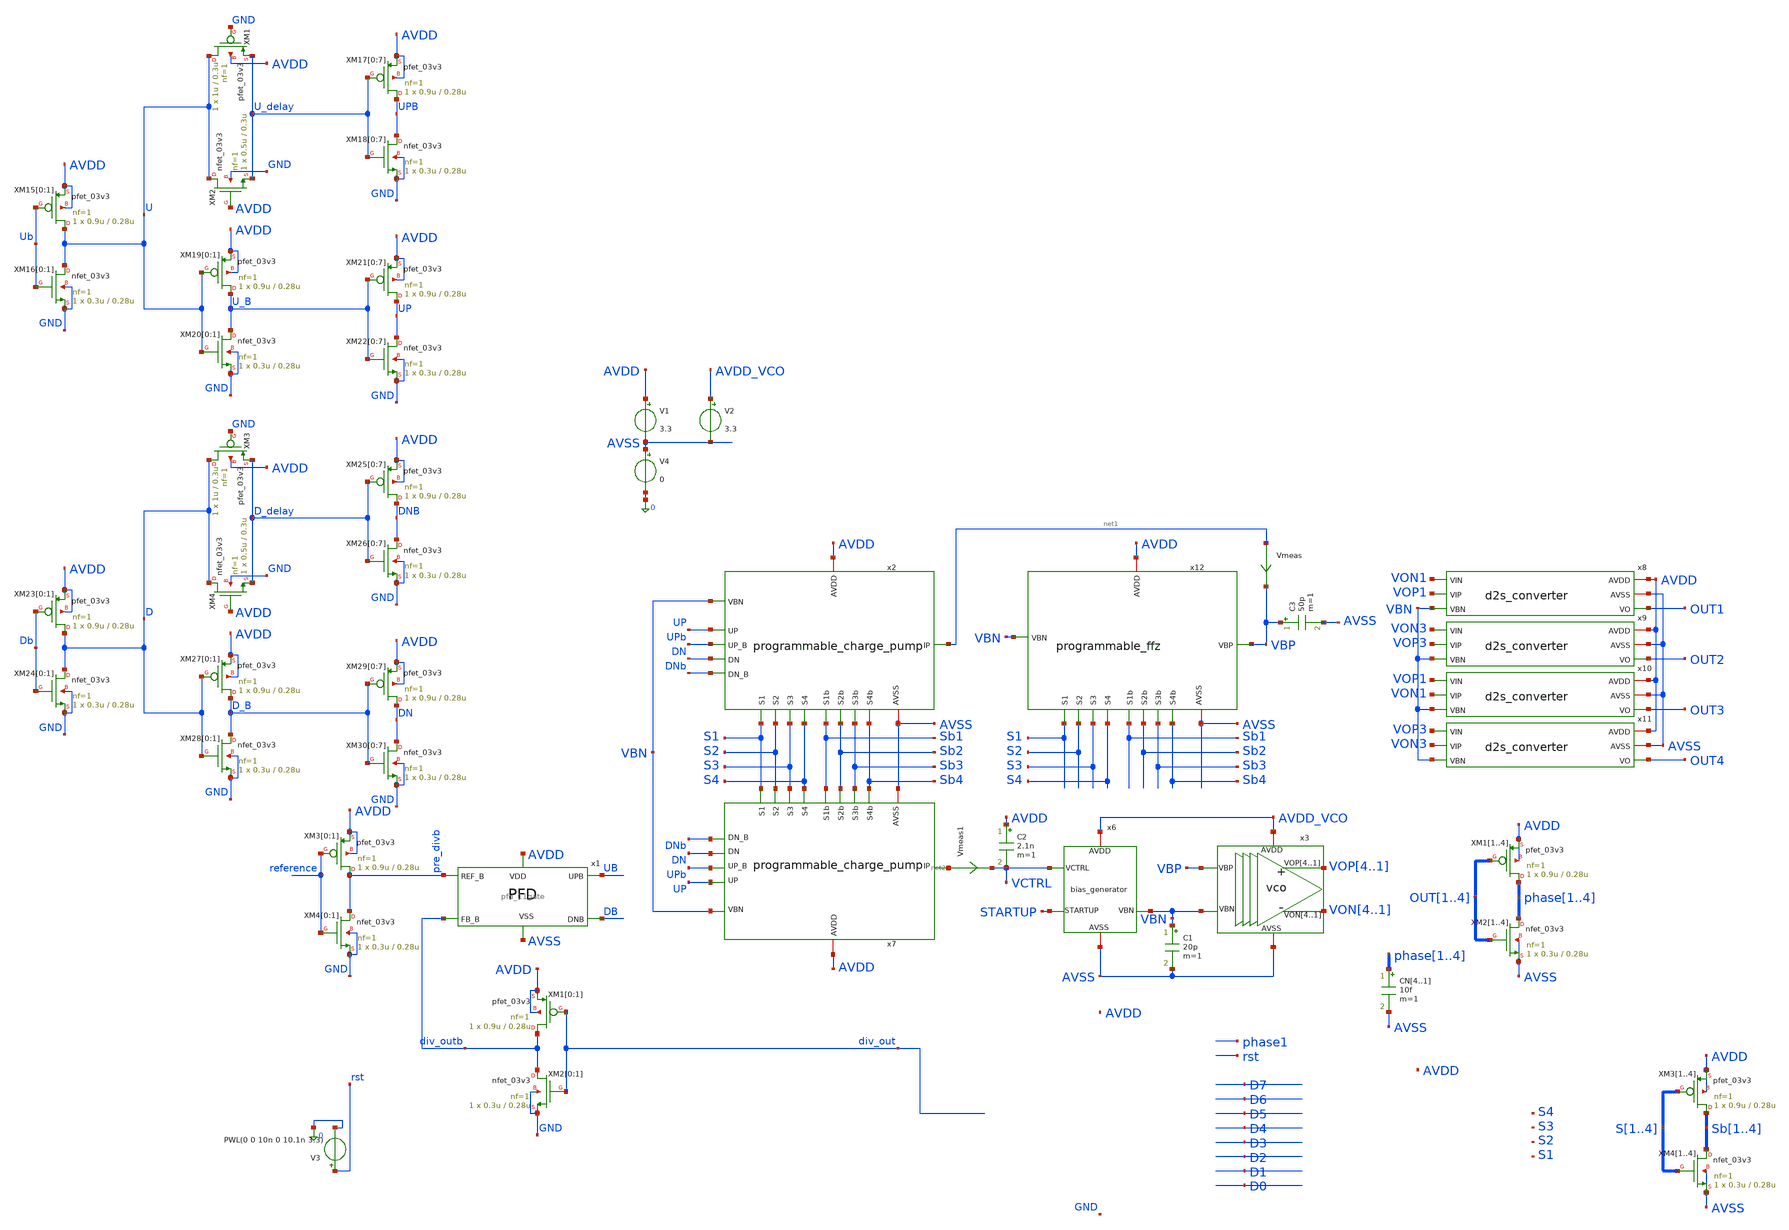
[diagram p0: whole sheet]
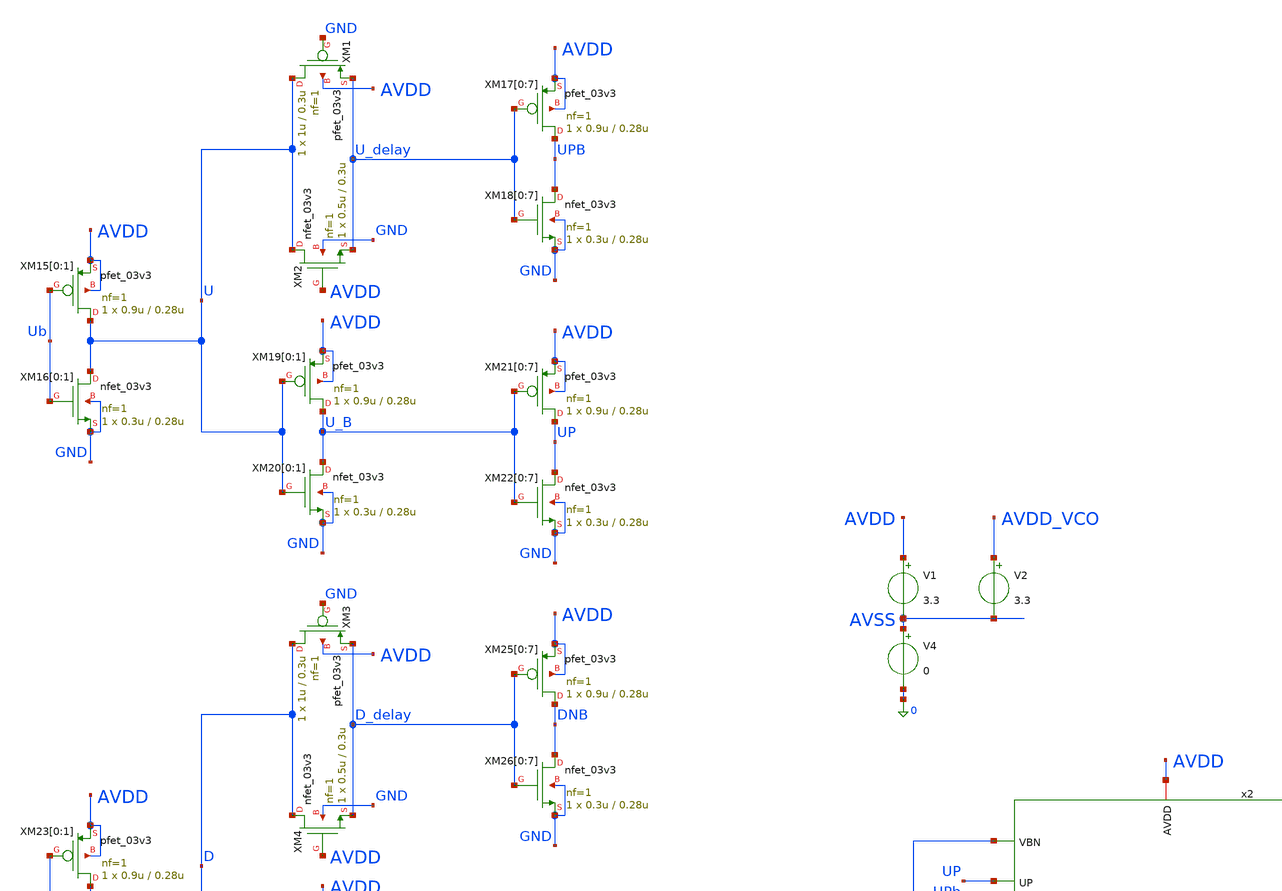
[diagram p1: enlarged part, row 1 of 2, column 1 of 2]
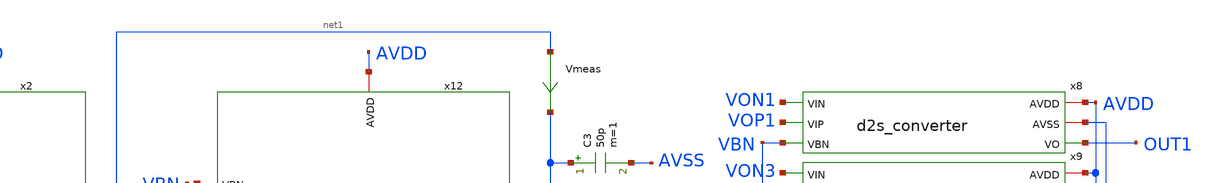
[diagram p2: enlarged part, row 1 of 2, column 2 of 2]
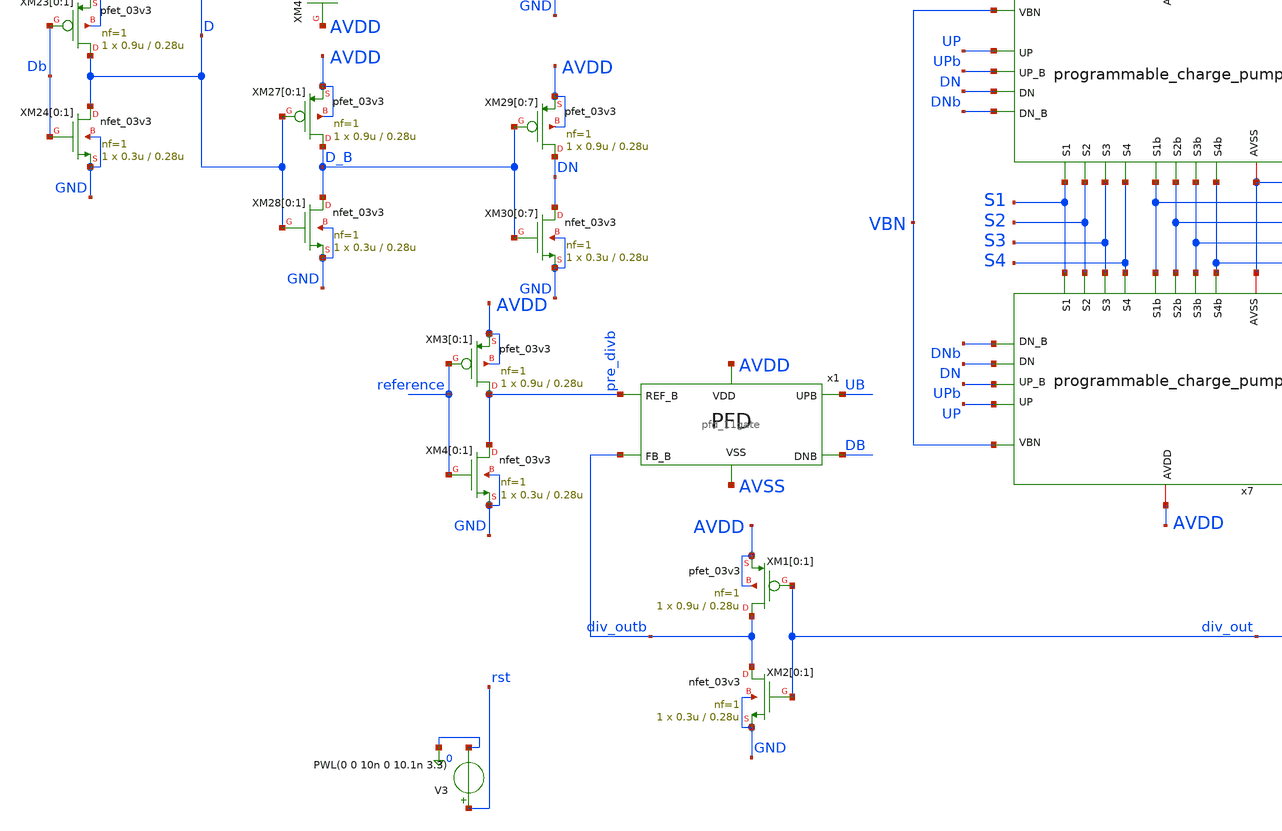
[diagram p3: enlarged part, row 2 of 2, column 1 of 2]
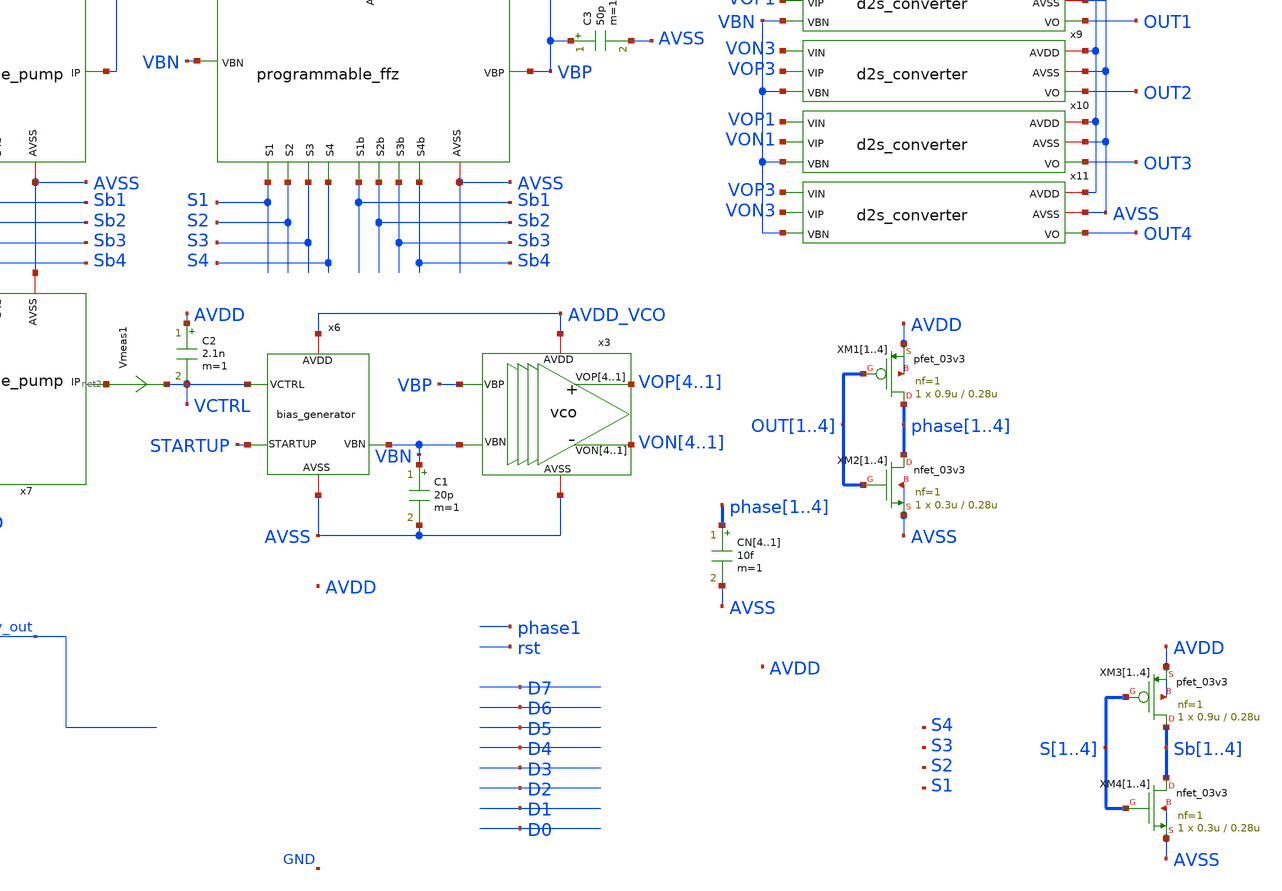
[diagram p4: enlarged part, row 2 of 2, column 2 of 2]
** sch_path: designs/untitled-2.sch
**.subckt untitled-2
x3 VOP4 VOP3 VOP2 VOP1 VON4 VON3 VON2 VON1 AVDD_VCO AVSS VBP VBN vco
x6 VCTRL AVDD_VCO STARTUP AVSS VBN bias_generator
C2 AVDD VCTRL 2.1n m=1
x8 AVDD AVSS VON1 VOP1 VBN OUT1 d2s_converter
XM11 phase1 OUT1 AVDD AVDD pfet_03v3 L=0.28u W=0.9u nf=1 ad='int((nf+1)/2) * W/nf * 0.18u' as='int((nf+2)/2) * W/nf * 0.18u'
+ pd='2*int((nf+1)/2) * (W/nf + 0.18u)' ps='2*int((nf+2)/2) * (W/nf + 0.18u)' nrd='0.18u / W' nrs='0.18u / W'
+ sa=0 sb=0 sd=0 m=1
XM12 phase2 OUT2 AVDD AVDD pfet_03v3 L=0.28u W=0.9u nf=1 ad='int((nf+1)/2) * W/nf * 0.18u' as='int((nf+2)/2) * W/nf * 0.18u'
+ pd='2*int((nf+1)/2) * (W/nf + 0.18u)' ps='2*int((nf+2)/2) * (W/nf + 0.18u)' nrd='0.18u / W' nrs='0.18u / W'
+ sa=0 sb=0 sd=0 m=1
XM13 phase3 OUT3 AVDD AVDD pfet_03v3 L=0.28u W=0.9u nf=1 ad='int((nf+1)/2) * W/nf * 0.18u' as='int((nf+2)/2) * W/nf * 0.18u'
+ pd='2*int((nf+1)/2) * (W/nf + 0.18u)' ps='2*int((nf+2)/2) * (W/nf + 0.18u)' nrd='0.18u / W' nrs='0.18u / W'
+ sa=0 sb=0 sd=0 m=1
XM14 phase4 OUT4 AVDD AVDD pfet_03v3 L=0.28u W=0.9u nf=1 ad='int((nf+1)/2) * W/nf * 0.18u' as='int((nf+2)/2) * W/nf * 0.18u'
+ pd='2*int((nf+1)/2) * (W/nf + 0.18u)' ps='2*int((nf+2)/2) * (W/nf + 0.18u)' nrd='0.18u / W' nrs='0.18u / W'
+ sa=0 sb=0 sd=0 m=1
XM21 phase1 OUT1 AVSS AVSS nfet_03v3 L=0.28u W=0.3u nf=1 ad='int((nf+1)/2) * W/nf * 0.18u' as='int((nf+2)/2) * W/nf * 0.18u'
+ pd='2*int((nf+1)/2) * (W/nf + 0.18u)' ps='2*int((nf+2)/2) * (W/nf + 0.18u)' nrd='0.18u / W' nrs='0.18u / W'
+ sa=0 sb=0 sd=0 m=1
XM22 phase2 OUT2 AVSS AVSS nfet_03v3 L=0.28u W=0.3u nf=1 ad='int((nf+1)/2) * W/nf * 0.18u' as='int((nf+2)/2) * W/nf * 0.18u'
+ pd='2*int((nf+1)/2) * (W/nf + 0.18u)' ps='2*int((nf+2)/2) * (W/nf + 0.18u)' nrd='0.18u / W' nrs='0.18u / W'
+ sa=0 sb=0 sd=0 m=1
XM23 phase3 OUT3 AVSS AVSS nfet_03v3 L=0.28u W=0.3u nf=1 ad='int((nf+1)/2) * W/nf * 0.18u' as='int((nf+2)/2) * W/nf * 0.18u'
+ pd='2*int((nf+1)/2) * (W/nf + 0.18u)' ps='2*int((nf+2)/2) * (W/nf + 0.18u)' nrd='0.18u / W' nrs='0.18u / W'
+ sa=0 sb=0 sd=0 m=1
XM24 phase4 OUT4 AVSS AVSS nfet_03v3 L=0.28u W=0.3u nf=1 ad='int((nf+1)/2) * W/nf * 0.18u' as='int((nf+2)/2) * W/nf * 0.18u'
+ pd='2*int((nf+1)/2) * (W/nf + 0.18u)' ps='2*int((nf+2)/2) * (W/nf + 0.18u)' nrd='0.18u / W' nrs='0.18u / W'
+ sa=0 sb=0 sd=0 m=1
x9 AVDD AVSS VON3 VOP3 VBN OUT2 d2s_converter
x10 AVDD AVSS VOP1 VON1 VBN OUT3 d2s_converter
x11 AVDD AVSS VOP3 VON3 VBN OUT4 d2s_converter
V1 AVDD AVSS 3.3
V4 AVSS 0 0
V2 AVDD_VCO AVSS 3.3
x2 AVSS AVDD UP UPb DN net1 DNb VBN Sb1 S1 Sb2 S2 Sb3 S3 Sb4 S4 programmable_charge_pump
x7 AVSS AVDD UP UPb DN net2 DNb VBN Sb1 S1 Sb2 S2 Sb3 S3 Sb4 S4 programmable_charge_pump
CN4 phase1 AVSS 10f m=1
CN3 phase2 AVSS 10f m=1
CN2 phase3 AVSS 10f m=1
CN1 phase4 AVSS 10f m=1
Vmeas net1 VBP 0
.save i(vmeas)
Vmeas1 net2 VCTRL 0
.save i(vmeas1)
C1 VBN AVSS 20p m=1
C3 VBP AVSS 50p m=1
x12 VBP AVSS AVDD VBN Sb1 S1 Sb2 S2 Sb3 S3 Sb4 S4 programmable_ffz
x1 pre_divb UB DB div_outb AVDD AVSS pfd_11gate
XM15[0] U Ub AVDD AVDD pfet_03v3 L=0.28u W=0.9u nf=1 ad='int((nf+1)/2) * W/nf * 0.18u' as='int((nf+2)/2) * W/nf * 0.18u'
+ pd='2*int((nf+1)/2) * (W/nf + 0.18u)' ps='2*int((nf+2)/2) * (W/nf + 0.18u)' nrd='0.18u / W' nrs='0.18u / W'
+ sa=0 sb=0 sd=0 m=1
XM15[1] U Ub AVDD AVDD pfet_03v3 L=0.28u W=0.9u nf=1 ad='int((nf+1)/2) * W/nf * 0.18u' as='int((nf+2)/2) * W/nf * 0.18u'
+ pd='2*int((nf+1)/2) * (W/nf + 0.18u)' ps='2*int((nf+2)/2) * (W/nf + 0.18u)' nrd='0.18u / W' nrs='0.18u / W'
+ sa=0 sb=0 sd=0 m=1
XM16[0] U Ub GND GND nfet_03v3 L=0.28u W=0.3u nf=1 ad='int((nf+1)/2) * W/nf * 0.18u' as='int((nf+2)/2) * W/nf * 0.18u'
+ pd='2*int((nf+1)/2) * (W/nf + 0.18u)' ps='2*int((nf+2)/2) * (W/nf + 0.18u)' nrd='0.18u / W' nrs='0.18u / W'
+ sa=0 sb=0 sd=0 m=1
XM16[1] U Ub GND GND nfet_03v3 L=0.28u W=0.3u nf=1 ad='int((nf+1)/2) * W/nf * 0.18u' as='int((nf+2)/2) * W/nf * 0.18u'
+ pd='2*int((nf+1)/2) * (W/nf + 0.18u)' ps='2*int((nf+2)/2) * (W/nf + 0.18u)' nrd='0.18u / W' nrs='0.18u / W'
+ sa=0 sb=0 sd=0 m=1
XM1 U GND U_delay AVDD pfet_03v3 L=0.3u W=1u nf=1 ad='int((nf+1)/2) * W/nf * 0.18u' as='int((nf+2)/2) * W/nf * 0.18u'
+ pd='2*int((nf+1)/2) * (W/nf + 0.18u)' ps='2*int((nf+2)/2) * (W/nf + 0.18u)' nrd='0.18u / W' nrs='0.18u / W'
+ sa=0 sb=0 sd=0 m=1
XM2 U AVDD U_delay GND nfet_03v3 L=0.3u W=0.5u nf=1 ad='int((nf+1)/2) * W/nf * 0.18u' as='int((nf+2)/2) * W/nf * 0.18u'
+ pd='2*int((nf+1)/2) * (W/nf + 0.18u)' ps='2*int((nf+2)/2) * (W/nf + 0.18u)' nrd='0.18u / W' nrs='0.18u / W'
+ sa=0 sb=0 sd=0 m=1
XM17[0] UPB U_delay AVDD AVDD pfet_03v3 L=0.28u W=0.9u nf=1 ad='int((nf+1)/2) * W/nf * 0.18u' as='int((nf+2)/2) * W/nf * 0.18u'
+ pd='2*int((nf+1)/2) * (W/nf + 0.18u)' ps='2*int((nf+2)/2) * (W/nf + 0.18u)' nrd='0.18u / W' nrs='0.18u / W'
+ sa=0 sb=0 sd=0 m=1
XM17[1] UPB U_delay AVDD AVDD pfet_03v3 L=0.28u W=0.9u nf=1 ad='int((nf+1)/2) * W/nf * 0.18u' as='int((nf+2)/2) * W/nf * 0.18u'
+ pd='2*int((nf+1)/2) * (W/nf + 0.18u)' ps='2*int((nf+2)/2) * (W/nf + 0.18u)' nrd='0.18u / W' nrs='0.18u / W'
+ sa=0 sb=0 sd=0 m=1
XM17[2] UPB U_delay AVDD AVDD pfet_03v3 L=0.28u W=0.9u nf=1 ad='int((nf+1)/2) * W/nf * 0.18u' as='int((nf+2)/2) * W/nf * 0.18u'
+ pd='2*int((nf+1)/2) * (W/nf + 0.18u)' ps='2*int((nf+2)/2) * (W/nf + 0.18u)' nrd='0.18u / W' nrs='0.18u / W'
+ sa=0 sb=0 sd=0 m=1
XM17[3] UPB U_delay AVDD AVDD pfet_03v3 L=0.28u W=0.9u nf=1 ad='int((nf+1)/2) * W/nf * 0.18u' as='int((nf+2)/2) * W/nf * 0.18u'
+ pd='2*int((nf+1)/2) * (W/nf + 0.18u)' ps='2*int((nf+2)/2) * (W/nf + 0.18u)' nrd='0.18u / W' nrs='0.18u / W'
+ sa=0 sb=0 sd=0 m=1
XM17[4] UPB U_delay AVDD AVDD pfet_03v3 L=0.28u W=0.9u nf=1 ad='int((nf+1)/2) * W/nf * 0.18u' as='int((nf+2)/2) * W/nf * 0.18u'
+ pd='2*int((nf+1)/2) * (W/nf + 0.18u)' ps='2*int((nf+2)/2) * (W/nf + 0.18u)' nrd='0.18u / W' nrs='0.18u / W'
+ sa=0 sb=0 sd=0 m=1
XM17[5] UPB U_delay AVDD AVDD pfet_03v3 L=0.28u W=0.9u nf=1 ad='int((nf+1)/2) * W/nf * 0.18u' as='int((nf+2)/2) * W/nf * 0.18u'
+ pd='2*int((nf+1)/2) * (W/nf + 0.18u)' ps='2*int((nf+2)/2) * (W/nf + 0.18u)' nrd='0.18u / W' nrs='0.18u / W'
+ sa=0 sb=0 sd=0 m=1
XM17[6] UPB U_delay AVDD AVDD pfet_03v3 L=0.28u W=0.9u nf=1 ad='int((nf+1)/2) * W/nf * 0.18u' as='int((nf+2)/2) * W/nf * 0.18u'
+ pd='2*int((nf+1)/2) * (W/nf + 0.18u)' ps='2*int((nf+2)/2) * (W/nf + 0.18u)' nrd='0.18u / W' nrs='0.18u / W'
+ sa=0 sb=0 sd=0 m=1
XM17[7] UPB U_delay AVDD AVDD pfet_03v3 L=0.28u W=0.9u nf=1 ad='int((nf+1)/2) * W/nf * 0.18u' as='int((nf+2)/2) * W/nf * 0.18u'
+ pd='2*int((nf+1)/2) * (W/nf + 0.18u)' ps='2*int((nf+2)/2) * (W/nf + 0.18u)' nrd='0.18u / W' nrs='0.18u / W'
+ sa=0 sb=0 sd=0 m=1
XM18[0] UPB U_delay GND GND nfet_03v3 L=0.28u W=0.3u nf=1 ad='int((nf+1)/2) * W/nf * 0.18u' as='int((nf+2)/2) * W/nf * 0.18u'
+ pd='2*int((nf+1)/2) * (W/nf + 0.18u)' ps='2*int((nf+2)/2) * (W/nf + 0.18u)' nrd='0.18u / W' nrs='0.18u / W'
+ sa=0 sb=0 sd=0 m=1
XM18[1] UPB U_delay GND GND nfet_03v3 L=0.28u W=0.3u nf=1 ad='int((nf+1)/2) * W/nf * 0.18u' as='int((nf+2)/2) * W/nf * 0.18u'
+ pd='2*int((nf+1)/2) * (W/nf + 0.18u)' ps='2*int((nf+2)/2) * (W/nf + 0.18u)' nrd='0.18u / W' nrs='0.18u / W'
+ sa=0 sb=0 sd=0 m=1
XM18[2] UPB U_delay GND GND nfet_03v3 L=0.28u W=0.3u nf=1 ad='int((nf+1)/2) * W/nf * 0.18u' as='int((nf+2)/2) * W/nf * 0.18u'
+ pd='2*int((nf+1)/2) * (W/nf + 0.18u)' ps='2*int((nf+2)/2) * (W/nf + 0.18u)' nrd='0.18u / W' nrs='0.18u / W'
+ sa=0 sb=0 sd=0 m=1
XM18[3] UPB U_delay GND GND nfet_03v3 L=0.28u W=0.3u nf=1 ad='int((nf+1)/2) * W/nf * 0.18u' as='int((nf+2)/2) * W/nf * 0.18u'
+ pd='2*int((nf+1)/2) * (W/nf + 0.18u)' ps='2*int((nf+2)/2) * (W/nf + 0.18u)' nrd='0.18u / W' nrs='0.18u / W'
+ sa=0 sb=0 sd=0 m=1
XM18[4] UPB U_delay GND GND nfet_03v3 L=0.28u W=0.3u nf=1 ad='int((nf+1)/2) * W/nf * 0.18u' as='int((nf+2)/2) * W/nf * 0.18u'
+ pd='2*int((nf+1)/2) * (W/nf + 0.18u)' ps='2*int((nf+2)/2) * (W/nf + 0.18u)' nrd='0.18u / W' nrs='0.18u / W'
+ sa=0 sb=0 sd=0 m=1
XM18[5] UPB U_delay GND GND nfet_03v3 L=0.28u W=0.3u nf=1 ad='int((nf+1)/2) * W/nf * 0.18u' as='int((nf+2)/2) * W/nf * 0.18u'
+ pd='2*int((nf+1)/2) * (W/nf + 0.18u)' ps='2*int((nf+2)/2) * (W/nf + 0.18u)' nrd='0.18u / W' nrs='0.18u / W'
+ sa=0 sb=0 sd=0 m=1
XM18[6] UPB U_delay GND GND nfet_03v3 L=0.28u W=0.3u nf=1 ad='int((nf+1)/2) * W/nf * 0.18u' as='int((nf+2)/2) * W/nf * 0.18u'
+ pd='2*int((nf+1)/2) * (W/nf + 0.18u)' ps='2*int((nf+2)/2) * (W/nf + 0.18u)' nrd='0.18u / W' nrs='0.18u / W'
+ sa=0 sb=0 sd=0 m=1
XM18[7] UPB U_delay GND GND nfet_03v3 L=0.28u W=0.3u nf=1 ad='int((nf+1)/2) * W/nf * 0.18u' as='int((nf+2)/2) * W/nf * 0.18u'
+ pd='2*int((nf+1)/2) * (W/nf + 0.18u)' ps='2*int((nf+2)/2) * (W/nf + 0.18u)' nrd='0.18u / W' nrs='0.18u / W'
+ sa=0 sb=0 sd=0 m=1
XM19[0] U_B U AVDD AVDD pfet_03v3 L=0.28u W=0.9u nf=1 ad='int((nf+1)/2) * W/nf * 0.18u' as='int((nf+2)/2) * W/nf * 0.18u'
+ pd='2*int((nf+1)/2) * (W/nf + 0.18u)' ps='2*int((nf+2)/2) * (W/nf + 0.18u)' nrd='0.18u / W' nrs='0.18u / W'
+ sa=0 sb=0 sd=0 m=1
XM19[1] U_B U AVDD AVDD pfet_03v3 L=0.28u W=0.9u nf=1 ad='int((nf+1)/2) * W/nf * 0.18u' as='int((nf+2)/2) * W/nf * 0.18u'
+ pd='2*int((nf+1)/2) * (W/nf + 0.18u)' ps='2*int((nf+2)/2) * (W/nf + 0.18u)' nrd='0.18u / W' nrs='0.18u / W'
+ sa=0 sb=0 sd=0 m=1
XM20[0] U_B U GND GND nfet_03v3 L=0.28u W=0.3u nf=1 ad='int((nf+1)/2) * W/nf * 0.18u' as='int((nf+2)/2) * W/nf * 0.18u'
+ pd='2*int((nf+1)/2) * (W/nf + 0.18u)' ps='2*int((nf+2)/2) * (W/nf + 0.18u)' nrd='0.18u / W' nrs='0.18u / W'
+ sa=0 sb=0 sd=0 m=1
XM20[1] U_B U GND GND nfet_03v3 L=0.28u W=0.3u nf=1 ad='int((nf+1)/2) * W/nf * 0.18u' as='int((nf+2)/2) * W/nf * 0.18u'
+ pd='2*int((nf+1)/2) * (W/nf + 0.18u)' ps='2*int((nf+2)/2) * (W/nf + 0.18u)' nrd='0.18u / W' nrs='0.18u / W'
+ sa=0 sb=0 sd=0 m=1
XM21[0] UP U_B AVDD AVDD pfet_03v3 L=0.28u W=0.9u nf=1 ad='int((nf+1)/2) * W/nf * 0.18u' as='int((nf+2)/2) * W/nf * 0.18u'
+ pd='2*int((nf+1)/2) * (W/nf + 0.18u)' ps='2*int((nf+2)/2) * (W/nf + 0.18u)' nrd='0.18u / W' nrs='0.18u / W'
+ sa=0 sb=0 sd=0 m=1
XM21[1] UP U_B AVDD AVDD pfet_03v3 L=0.28u W=0.9u nf=1 ad='int((nf+1)/2) * W/nf * 0.18u' as='int((nf+2)/2) * W/nf * 0.18u'
+ pd='2*int((nf+1)/2) * (W/nf + 0.18u)' ps='2*int((nf+2)/2) * (W/nf + 0.18u)' nrd='0.18u / W' nrs='0.18u / W'
+ sa=0 sb=0 sd=0 m=1
XM21[2] UP U_B AVDD AVDD pfet_03v3 L=0.28u W=0.9u nf=1 ad='int((nf+1)/2) * W/nf * 0.18u' as='int((nf+2)/2) * W/nf * 0.18u'
+ pd='2*int((nf+1)/2) * (W/nf + 0.18u)' ps='2*int((nf+2)/2) * (W/nf + 0.18u)' nrd='0.18u / W' nrs='0.18u / W'
+ sa=0 sb=0 sd=0 m=1
XM21[3] UP U_B AVDD AVDD pfet_03v3 L=0.28u W=0.9u nf=1 ad='int((nf+1)/2) * W/nf * 0.18u' as='int((nf+2)/2) * W/nf * 0.18u'
+ pd='2*int((nf+1)/2) * (W/nf + 0.18u)' ps='2*int((nf+2)/2) * (W/nf + 0.18u)' nrd='0.18u / W' nrs='0.18u / W'
+ sa=0 sb=0 sd=0 m=1
XM21[4] UP U_B AVDD AVDD pfet_03v3 L=0.28u W=0.9u nf=1 ad='int((nf+1)/2) * W/nf * 0.18u' as='int((nf+2)/2) * W/nf * 0.18u'
+ pd='2*int((nf+1)/2) * (W/nf + 0.18u)' ps='2*int((nf+2)/2) * (W/nf + 0.18u)' nrd='0.18u / W' nrs='0.18u / W'
+ sa=0 sb=0 sd=0 m=1
XM21[5] UP U_B AVDD AVDD pfet_03v3 L=0.28u W=0.9u nf=1 ad='int((nf+1)/2) * W/nf * 0.18u' as='int((nf+2)/2) * W/nf * 0.18u'
+ pd='2*int((nf+1)/2) * (W/nf + 0.18u)' ps='2*int((nf+2)/2) * (W/nf + 0.18u)' nrd='0.18u / W' nrs='0.18u / W'
+ sa=0 sb=0 sd=0 m=1
XM21[6] UP U_B AVDD AVDD pfet_03v3 L=0.28u W=0.9u nf=1 ad='int((nf+1)/2) * W/nf * 0.18u' as='int((nf+2)/2) * W/nf * 0.18u'
+ pd='2*int((nf+1)/2) * (W/nf + 0.18u)' ps='2*int((nf+2)/2) * (W/nf + 0.18u)' nrd='0.18u / W' nrs='0.18u / W'
+ sa=0 sb=0 sd=0 m=1
XM21[7] UP U_B AVDD AVDD pfet_03v3 L=0.28u W=0.9u nf=1 ad='int((nf+1)/2) * W/nf * 0.18u' as='int((nf+2)/2) * W/nf * 0.18u'
+ pd='2*int((nf+1)/2) * (W/nf + 0.18u)' ps='2*int((nf+2)/2) * (W/nf + 0.18u)' nrd='0.18u / W' nrs='0.18u / W'
+ sa=0 sb=0 sd=0 m=1
XM22[0] UP U_B GND GND nfet_03v3 L=0.28u W=0.3u nf=1 ad='int((nf+1)/2) * W/nf * 0.18u' as='int((nf+2)/2) * W/nf * 0.18u'
+ pd='2*int((nf+1)/2) * (W/nf + 0.18u)' ps='2*int((nf+2)/2) * (W/nf + 0.18u)' nrd='0.18u / W' nrs='0.18u / W'
+ sa=0 sb=0 sd=0 m=1
XM22[1] UP U_B GND GND nfet_03v3 L=0.28u W=0.3u nf=1 ad='int((nf+1)/2) * W/nf * 0.18u' as='int((nf+2)/2) * W/nf * 0.18u'
+ pd='2*int((nf+1)/2) * (W/nf + 0.18u)' ps='2*int((nf+2)/2) * (W/nf + 0.18u)' nrd='0.18u / W' nrs='0.18u / W'
+ sa=0 sb=0 sd=0 m=1
XM22[2] UP U_B GND GND nfet_03v3 L=0.28u W=0.3u nf=1 ad='int((nf+1)/2) * W/nf * 0.18u' as='int((nf+2)/2) * W/nf * 0.18u'
+ pd='2*int((nf+1)/2) * (W/nf + 0.18u)' ps='2*int((nf+2)/2) * (W/nf + 0.18u)' nrd='0.18u / W' nrs='0.18u / W'
+ sa=0 sb=0 sd=0 m=1
XM22[3] UP U_B GND GND nfet_03v3 L=0.28u W=0.3u nf=1 ad='int((nf+1)/2) * W/nf * 0.18u' as='int((nf+2)/2) * W/nf * 0.18u'
+ pd='2*int((nf+1)/2) * (W/nf + 0.18u)' ps='2*int((nf+2)/2) * (W/nf + 0.18u)' nrd='0.18u / W' nrs='0.18u / W'
+ sa=0 sb=0 sd=0 m=1
XM22[4] UP U_B GND GND nfet_03v3 L=0.28u W=0.3u nf=1 ad='int((nf+1)/2) * W/nf * 0.18u' as='int((nf+2)/2) * W/nf * 0.18u'
+ pd='2*int((nf+1)/2) * (W/nf + 0.18u)' ps='2*int((nf+2)/2) * (W/nf + 0.18u)' nrd='0.18u / W' nrs='0.18u / W'
+ sa=0 sb=0 sd=0 m=1
XM22[5] UP U_B GND GND nfet_03v3 L=0.28u W=0.3u nf=1 ad='int((nf+1)/2) * W/nf * 0.18u' as='int((nf+2)/2) * W/nf * 0.18u'
+ pd='2*int((nf+1)/2) * (W/nf + 0.18u)' ps='2*int((nf+2)/2) * (W/nf + 0.18u)' nrd='0.18u / W' nrs='0.18u / W'
+ sa=0 sb=0 sd=0 m=1
XM22[6] UP U_B GND GND nfet_03v3 L=0.28u W=0.3u nf=1 ad='int((nf+1)/2) * W/nf * 0.18u' as='int((nf+2)/2) * W/nf * 0.18u'
+ pd='2*int((nf+1)/2) * (W/nf + 0.18u)' ps='2*int((nf+2)/2) * (W/nf + 0.18u)' nrd='0.18u / W' nrs='0.18u / W'
+ sa=0 sb=0 sd=0 m=1
XM22[7] UP U_B GND GND nfet_03v3 L=0.28u W=0.3u nf=1 ad='int((nf+1)/2) * W/nf * 0.18u' as='int((nf+2)/2) * W/nf * 0.18u'
+ pd='2*int((nf+1)/2) * (W/nf + 0.18u)' ps='2*int((nf+2)/2) * (W/nf + 0.18u)' nrd='0.18u / W' nrs='0.18u / W'
+ sa=0 sb=0 sd=0 m=1
XM23[0] D Db AVDD AVDD pfet_03v3 L=0.28u W=0.9u nf=1 ad='int((nf+1)/2) * W/nf * 0.18u' as='int((nf+2)/2) * W/nf * 0.18u'
+ pd='2*int((nf+1)/2) * (W/nf + 0.18u)' ps='2*int((nf+2)/2) * (W/nf + 0.18u)' nrd='0.18u / W' nrs='0.18u / W'
+ sa=0 sb=0 sd=0 m=1
XM23[1] D Db AVDD AVDD pfet_03v3 L=0.28u W=0.9u nf=1 ad='int((nf+1)/2) * W/nf * 0.18u' as='int((nf+2)/2) * W/nf * 0.18u'
+ pd='2*int((nf+1)/2) * (W/nf + 0.18u)' ps='2*int((nf+2)/2) * (W/nf + 0.18u)' nrd='0.18u / W' nrs='0.18u / W'
+ sa=0 sb=0 sd=0 m=1
XM24[0] D Db GND GND nfet_03v3 L=0.28u W=0.3u nf=1 ad='int((nf+1)/2) * W/nf * 0.18u' as='int((nf+2)/2) * W/nf * 0.18u'
+ pd='2*int((nf+1)/2) * (W/nf + 0.18u)' ps='2*int((nf+2)/2) * (W/nf + 0.18u)' nrd='0.18u / W' nrs='0.18u / W'
+ sa=0 sb=0 sd=0 m=1
XM24[1] D Db GND GND nfet_03v3 L=0.28u W=0.3u nf=1 ad='int((nf+1)/2) * W/nf * 0.18u' as='int((nf+2)/2) * W/nf * 0.18u'
+ pd='2*int((nf+1)/2) * (W/nf + 0.18u)' ps='2*int((nf+2)/2) * (W/nf + 0.18u)' nrd='0.18u / W' nrs='0.18u / W'
+ sa=0 sb=0 sd=0 m=1
XM25[0] DNB D_delay AVDD AVDD pfet_03v3 L=0.28u W=0.9u nf=1 ad='int((nf+1)/2) * W/nf * 0.18u' as='int((nf+2)/2) * W/nf * 0.18u'
+ pd='2*int((nf+1)/2) * (W/nf + 0.18u)' ps='2*int((nf+2)/2) * (W/nf + 0.18u)' nrd='0.18u / W' nrs='0.18u / W'
+ sa=0 sb=0 sd=0 m=1
XM25[1] DNB D_delay AVDD AVDD pfet_03v3 L=0.28u W=0.9u nf=1 ad='int((nf+1)/2) * W/nf * 0.18u' as='int((nf+2)/2) * W/nf * 0.18u'
+ pd='2*int((nf+1)/2) * (W/nf + 0.18u)' ps='2*int((nf+2)/2) * (W/nf + 0.18u)' nrd='0.18u / W' nrs='0.18u / W'
+ sa=0 sb=0 sd=0 m=1
XM25[2] DNB D_delay AVDD AVDD pfet_03v3 L=0.28u W=0.9u nf=1 ad='int((nf+1)/2) * W/nf * 0.18u' as='int((nf+2)/2) * W/nf * 0.18u'
+ pd='2*int((nf+1)/2) * (W/nf + 0.18u)' ps='2*int((nf+2)/2) * (W/nf + 0.18u)' nrd='0.18u / W' nrs='0.18u / W'
+ sa=0 sb=0 sd=0 m=1
XM25[3] DNB D_delay AVDD AVDD pfet_03v3 L=0.28u W=0.9u nf=1 ad='int((nf+1)/2) * W/nf * 0.18u' as='int((nf+2)/2) * W/nf * 0.18u'
+ pd='2*int((nf+1)/2) * (W/nf + 0.18u)' ps='2*int((nf+2)/2) * (W/nf + 0.18u)' nrd='0.18u / W' nrs='0.18u / W'
+ sa=0 sb=0 sd=0 m=1
XM25[4] DNB D_delay AVDD AVDD pfet_03v3 L=0.28u W=0.9u nf=1 ad='int((nf+1)/2) * W/nf * 0.18u' as='int((nf+2)/2) * W/nf * 0.18u'
+ pd='2*int((nf+1)/2) * (W/nf + 0.18u)' ps='2*int((nf+2)/2) * (W/nf + 0.18u)' nrd='0.18u / W' nrs='0.18u / W'
+ sa=0 sb=0 sd=0 m=1
XM25[5] DNB D_delay AVDD AVDD pfet_03v3 L=0.28u W=0.9u nf=1 ad='int((nf+1)/2) * W/nf * 0.18u' as='int((nf+2)/2) * W/nf * 0.18u'
+ pd='2*int((nf+1)/2) * (W/nf + 0.18u)' ps='2*int((nf+2)/2) * (W/nf + 0.18u)' nrd='0.18u / W' nrs='0.18u / W'
+ sa=0 sb=0 sd=0 m=1
XM25[6] DNB D_delay AVDD AVDD pfet_03v3 L=0.28u W=0.9u nf=1 ad='int((nf+1)/2) * W/nf * 0.18u' as='int((nf+2)/2) * W/nf * 0.18u'
+ pd='2*int((nf+1)/2) * (W/nf + 0.18u)' ps='2*int((nf+2)/2) * (W/nf + 0.18u)' nrd='0.18u / W' nrs='0.18u / W'
+ sa=0 sb=0 sd=0 m=1
XM25[7] DNB D_delay AVDD AVDD pfet_03v3 L=0.28u W=0.9u nf=1 ad='int((nf+1)/2) * W/nf * 0.18u' as='int((nf+2)/2) * W/nf * 0.18u'
+ pd='2*int((nf+1)/2) * (W/nf + 0.18u)' ps='2*int((nf+2)/2) * (W/nf + 0.18u)' nrd='0.18u / W' nrs='0.18u / W'
+ sa=0 sb=0 sd=0 m=1
XM26[0] DNB D_delay GND GND nfet_03v3 L=0.28u W=0.3u nf=1 ad='int((nf+1)/2) * W/nf * 0.18u' as='int((nf+2)/2) * W/nf * 0.18u'
+ pd='2*int((nf+1)/2) * (W/nf + 0.18u)' ps='2*int((nf+2)/2) * (W/nf + 0.18u)' nrd='0.18u / W' nrs='0.18u / W'
+ sa=0 sb=0 sd=0 m=1
XM26[1] DNB D_delay GND GND nfet_03v3 L=0.28u W=0.3u nf=1 ad='int((nf+1)/2) * W/nf * 0.18u' as='int((nf+2)/2) * W/nf * 0.18u'
+ pd='2*int((nf+1)/2) * (W/nf + 0.18u)' ps='2*int((nf+2)/2) * (W/nf + 0.18u)' nrd='0.18u / W' nrs='0.18u / W'
+ sa=0 sb=0 sd=0 m=1
XM26[2] DNB D_delay GND GND nfet_03v3 L=0.28u W=0.3u nf=1 ad='int((nf+1)/2) * W/nf * 0.18u' as='int((nf+2)/2) * W/nf * 0.18u'
+ pd='2*int((nf+1)/2) * (W/nf + 0.18u)' ps='2*int((nf+2)/2) * (W/nf + 0.18u)' nrd='0.18u / W' nrs='0.18u / W'
+ sa=0 sb=0 sd=0 m=1
XM26[3] DNB D_delay GND GND nfet_03v3 L=0.28u W=0.3u nf=1 ad='int((nf+1)/2) * W/nf * 0.18u' as='int((nf+2)/2) * W/nf * 0.18u'
+ pd='2*int((nf+1)/2) * (W/nf + 0.18u)' ps='2*int((nf+2)/2) * (W/nf + 0.18u)' nrd='0.18u / W' nrs='0.18u / W'
+ sa=0 sb=0 sd=0 m=1
XM26[4] DNB D_delay GND GND nfet_03v3 L=0.28u W=0.3u nf=1 ad='int((nf+1)/2) * W/nf * 0.18u' as='int((nf+2)/2) * W/nf * 0.18u'
+ pd='2*int((nf+1)/2) * (W/nf + 0.18u)' ps='2*int((nf+2)/2) * (W/nf + 0.18u)' nrd='0.18u / W' nrs='0.18u / W'
+ sa=0 sb=0 sd=0 m=1
XM26[5] DNB D_delay GND GND nfet_03v3 L=0.28u W=0.3u nf=1 ad='int((nf+1)/2) * W/nf * 0.18u' as='int((nf+2)/2) * W/nf * 0.18u'
+ pd='2*int((nf+1)/2) * (W/nf + 0.18u)' ps='2*int((nf+2)/2) * (W/nf + 0.18u)' nrd='0.18u / W' nrs='0.18u / W'
+ sa=0 sb=0 sd=0 m=1
XM26[6] DNB D_delay GND GND nfet_03v3 L=0.28u W=0.3u nf=1 ad='int((nf+1)/2) * W/nf * 0.18u' as='int((nf+2)/2) * W/nf * 0.18u'
+ pd='2*int((nf+1)/2) * (W/nf + 0.18u)' ps='2*int((nf+2)/2) * (W/nf + 0.18u)' nrd='0.18u / W' nrs='0.18u / W'
+ sa=0 sb=0 sd=0 m=1
XM26[7] DNB D_delay GND GND nfet_03v3 L=0.28u W=0.3u nf=1 ad='int((nf+1)/2) * W/nf * 0.18u' as='int((nf+2)/2) * W/nf * 0.18u'
+ pd='2*int((nf+1)/2) * (W/nf + 0.18u)' ps='2*int((nf+2)/2) * (W/nf + 0.18u)' nrd='0.18u / W' nrs='0.18u / W'
+ sa=0 sb=0 sd=0 m=1
XM27[0] D_B D AVDD AVDD pfet_03v3 L=0.28u W=0.9u nf=1 ad='int((nf+1)/2) * W/nf * 0.18u' as='int((nf+2)/2) * W/nf * 0.18u'
+ pd='2*int((nf+1)/2) * (W/nf + 0.18u)' ps='2*int((nf+2)/2) * (W/nf + 0.18u)' nrd='0.18u / W' nrs='0.18u / W'
+ sa=0 sb=0 sd=0 m=1
XM27[1] D_B D AVDD AVDD pfet_03v3 L=0.28u W=0.9u nf=1 ad='int((nf+1)/2) * W/nf * 0.18u' as='int((nf+2)/2) * W/nf * 0.18u'
+ pd='2*int((nf+1)/2) * (W/nf + 0.18u)' ps='2*int((nf+2)/2) * (W/nf + 0.18u)' nrd='0.18u / W' nrs='0.18u / W'
+ sa=0 sb=0 sd=0 m=1
XM28[0] D_B D GND GND nfet_03v3 L=0.28u W=0.3u nf=1 ad='int((nf+1)/2) * W/nf * 0.18u' as='int((nf+2)/2) * W/nf * 0.18u'
+ pd='2*int((nf+1)/2) * (W/nf + 0.18u)' ps='2*int((nf+2)/2) * (W/nf + 0.18u)' nrd='0.18u / W' nrs='0.18u / W'
+ sa=0 sb=0 sd=0 m=1
XM28[1] D_B D GND GND nfet_03v3 L=0.28u W=0.3u nf=1 ad='int((nf+1)/2) * W/nf * 0.18u' as='int((nf+2)/2) * W/nf * 0.18u'
+ pd='2*int((nf+1)/2) * (W/nf + 0.18u)' ps='2*int((nf+2)/2) * (W/nf + 0.18u)' nrd='0.18u / W' nrs='0.18u / W'
+ sa=0 sb=0 sd=0 m=1
XM29[0] DN D_B AVDD AVDD pfet_03v3 L=0.28u W=0.9u nf=1 ad='int((nf+1)/2) * W/nf * 0.18u' as='int((nf+2)/2) * W/nf * 0.18u'
+ pd='2*int((nf+1)/2) * (W/nf + 0.18u)' ps='2*int((nf+2)/2) * (W/nf + 0.18u)' nrd='0.18u / W' nrs='0.18u / W'
+ sa=0 sb=0 sd=0 m=1
XM29[1] DN D_B AVDD AVDD pfet_03v3 L=0.28u W=0.9u nf=1 ad='int((nf+1)/2) * W/nf * 0.18u' as='int((nf+2)/2) * W/nf * 0.18u'
+ pd='2*int((nf+1)/2) * (W/nf + 0.18u)' ps='2*int((nf+2)/2) * (W/nf + 0.18u)' nrd='0.18u / W' nrs='0.18u / W'
+ sa=0 sb=0 sd=0 m=1
XM29[2] DN D_B AVDD AVDD pfet_03v3 L=0.28u W=0.9u nf=1 ad='int((nf+1)/2) * W/nf * 0.18u' as='int((nf+2)/2) * W/nf * 0.18u'
+ pd='2*int((nf+1)/2) * (W/nf + 0.18u)' ps='2*int((nf+2)/2) * (W/nf + 0.18u)' nrd='0.18u / W' nrs='0.18u / W'
+ sa=0 sb=0 sd=0 m=1
XM29[3] DN D_B AVDD AVDD pfet_03v3 L=0.28u W=0.9u nf=1 ad='int((nf+1)/2) * W/nf * 0.18u' as='int((nf+2)/2) * W/nf * 0.18u'
+ pd='2*int((nf+1)/2) * (W/nf + 0.18u)' ps='2*int((nf+2)/2) * (W/nf + 0.18u)' nrd='0.18u / W' nrs='0.18u / W'
+ sa=0 sb=0 sd=0 m=1
XM29[4] DN D_B AVDD AVDD pfet_03v3 L=0.28u W=0.9u nf=1 ad='int((nf+1)/2) * W/nf * 0.18u' as='int((nf+2)/2) * W/nf * 0.18u'
+ pd='2*int((nf+1)/2) * (W/nf + 0.18u)' ps='2*int((nf+2)/2) * (W/nf + 0.18u)' nrd='0.18u / W' nrs='0.18u / W'
+ sa=0 sb=0 sd=0 m=1
XM29[5] DN D_B AVDD AVDD pfet_03v3 L=0.28u W=0.9u nf=1 ad='int((nf+1)/2) * W/nf * 0.18u' as='int((nf+2)/2) * W/nf * 0.18u'
+ pd='2*int((nf+1)/2) * (W/nf + 0.18u)' ps='2*int((nf+2)/2) * (W/nf + 0.18u)' nrd='0.18u / W' nrs='0.18u / W'
+ sa=0 sb=0 sd=0 m=1
XM29[6] DN D_B AVDD AVDD pfet_03v3 L=0.28u W=0.9u nf=1 ad='int((nf+1)/2) * W/nf * 0.18u' as='int((nf+2)/2) * W/nf * 0.18u'
+ pd='2*int((nf+1)/2) * (W/nf + 0.18u)' ps='2*int((nf+2)/2) * (W/nf + 0.18u)' nrd='0.18u / W' nrs='0.18u / W'
+ sa=0 sb=0 sd=0 m=1
XM29[7] DN D_B AVDD AVDD pfet_03v3 L=0.28u W=0.9u nf=1 ad='int((nf+1)/2) * W/nf * 0.18u' as='int((nf+2)/2) * W/nf * 0.18u'
+ pd='2*int((nf+1)/2) * (W/nf + 0.18u)' ps='2*int((nf+2)/2) * (W/nf + 0.18u)' nrd='0.18u / W' nrs='0.18u / W'
+ sa=0 sb=0 sd=0 m=1
XM30[0] DN D_B GND GND nfet_03v3 L=0.28u W=0.3u nf=1 ad='int((nf+1)/2) * W/nf * 0.18u' as='int((nf+2)/2) * W/nf * 0.18u'
+ pd='2*int((nf+1)/2) * (W/nf + 0.18u)' ps='2*int((nf+2)/2) * (W/nf + 0.18u)' nrd='0.18u / W' nrs='0.18u / W'
+ sa=0 sb=0 sd=0 m=1
XM30[1] DN D_B GND GND nfet_03v3 L=0.28u W=0.3u nf=1 ad='int((nf+1)/2) * W/nf * 0.18u' as='int((nf+2)/2) * W/nf * 0.18u'
+ pd='2*int((nf+1)/2) * (W/nf + 0.18u)' ps='2*int((nf+2)/2) * (W/nf + 0.18u)' nrd='0.18u / W' nrs='0.18u / W'
+ sa=0 sb=0 sd=0 m=1
XM30[2] DN D_B GND GND nfet_03v3 L=0.28u W=0.3u nf=1 ad='int((nf+1)/2) * W/nf * 0.18u' as='int((nf+2)/2) * W/nf * 0.18u'
+ pd='2*int((nf+1)/2) * (W/nf + 0.18u)' ps='2*int((nf+2)/2) * (W/nf + 0.18u)' nrd='0.18u / W' nrs='0.18u / W'
+ sa=0 sb=0 sd=0 m=1
XM30[3] DN D_B GND GND nfet_03v3 L=0.28u W=0.3u nf=1 ad='int((nf+1)/2) * W/nf * 0.18u' as='int((nf+2)/2) * W/nf * 0.18u'
+ pd='2*int((nf+1)/2) * (W/nf + 0.18u)' ps='2*int((nf+2)/2) * (W/nf + 0.18u)' nrd='0.18u / W' nrs='0.18u / W'
+ sa=0 sb=0 sd=0 m=1
XM30[4] DN D_B GND GND nfet_03v3 L=0.28u W=0.3u nf=1 ad='int((nf+1)/2) * W/nf * 0.18u' as='int((nf+2)/2) * W/nf * 0.18u'
+ pd='2*int((nf+1)/2) * (W/nf + 0.18u)' ps='2*int((nf+2)/2) * (W/nf + 0.18u)' nrd='0.18u / W' nrs='0.18u / W'
+ sa=0 sb=0 sd=0 m=1
XM30[5] DN D_B GND GND nfet_03v3 L=0.28u W=0.3u nf=1 ad='int((nf+1)/2) * W/nf * 0.18u' as='int((nf+2)/2) * W/nf * 0.18u'
+ pd='2*int((nf+1)/2) * (W/nf + 0.18u)' ps='2*int((nf+2)/2) * (W/nf + 0.18u)' nrd='0.18u / W' nrs='0.18u / W'
+ sa=0 sb=0 sd=0 m=1
XM30[6] DN D_B GND GND nfet_03v3 L=0.28u W=0.3u nf=1 ad='int((nf+1)/2) * W/nf * 0.18u' as='int((nf+2)/2) * W/nf * 0.18u'
+ pd='2*int((nf+1)/2) * (W/nf + 0.18u)' ps='2*int((nf+2)/2) * (W/nf + 0.18u)' nrd='0.18u / W' nrs='0.18u / W'
+ sa=0 sb=0 sd=0 m=1
XM30[7] DN D_B GND GND nfet_03v3 L=0.28u W=0.3u nf=1 ad='int((nf+1)/2) * W/nf * 0.18u' as='int((nf+2)/2) * W/nf * 0.18u'
+ pd='2*int((nf+1)/2) * (W/nf + 0.18u)' ps='2*int((nf+2)/2) * (W/nf + 0.18u)' nrd='0.18u / W' nrs='0.18u / W'
+ sa=0 sb=0 sd=0 m=1
XM3 D GND D_delay AVDD pfet_03v3 L=0.3u W=1u nf=1 ad='int((nf+1)/2) * W/nf * 0.18u' as='int((nf+2)/2) * W/nf * 0.18u'
+ pd='2*int((nf+1)/2) * (W/nf + 0.18u)' ps='2*int((nf+2)/2) * (W/nf + 0.18u)' nrd='0.18u / W' nrs='0.18u / W'
+ sa=0 sb=0 sd=0 m=1
XM4 D AVDD D_delay GND nfet_03v3 L=0.3u W=0.5u nf=1 ad='int((nf+1)/2) * W/nf * 0.18u' as='int((nf+2)/2) * W/nf * 0.18u'
+ pd='2*int((nf+1)/2) * (W/nf + 0.18u)' ps='2*int((nf+2)/2) * (W/nf + 0.18u)' nrd='0.18u / W' nrs='0.18u / W'
+ sa=0 sb=0 sd=0 m=1
XM1[0] div_outb div_out AVDD AVDD pfet_03v3 L=0.28u W=0.9u nf=1 ad='int((nf+1)/2) * W/nf * 0.18u' as='int((nf+2)/2) * W/nf * 0.18u'
+ pd='2*int((nf+1)/2) * (W/nf + 0.18u)' ps='2*int((nf+2)/2) * (W/nf + 0.18u)' nrd='0.18u / W' nrs='0.18u / W'
+ sa=0 sb=0 sd=0 m=1
XM1[1] div_outb div_out AVDD AVDD pfet_03v3 L=0.28u W=0.9u nf=1 ad='int((nf+1)/2) * W/nf * 0.18u' as='int((nf+2)/2) * W/nf * 0.18u'
+ pd='2*int((nf+1)/2) * (W/nf + 0.18u)' ps='2*int((nf+2)/2) * (W/nf + 0.18u)' nrd='0.18u / W' nrs='0.18u / W'
+ sa=0 sb=0 sd=0 m=1
XM2[0] div_outb div_out GND GND nfet_03v3 L=0.28u W=0.3u nf=1 ad='int((nf+1)/2) * W/nf * 0.18u' as='int((nf+2)/2) * W/nf * 0.18u'
+ pd='2*int((nf+1)/2) * (W/nf + 0.18u)' ps='2*int((nf+2)/2) * (W/nf + 0.18u)' nrd='0.18u / W' nrs='0.18u / W'
+ sa=0 sb=0 sd=0 m=1
XM2[1] div_outb div_out GND GND nfet_03v3 L=0.28u W=0.3u nf=1 ad='int((nf+1)/2) * W/nf * 0.18u' as='int((nf+2)/2) * W/nf * 0.18u'
+ pd='2*int((nf+1)/2) * (W/nf + 0.18u)' ps='2*int((nf+2)/2) * (W/nf + 0.18u)' nrd='0.18u / W' nrs='0.18u / W'
+ sa=0 sb=0 sd=0 m=1
XM3[0] pre_divb reference AVDD AVDD pfet_03v3 L=0.28u W=0.9u nf=1 ad='int((nf+1)/2) * W/nf * 0.18u' as='int((nf+2)/2) * W/nf * 0.18u'
+ pd='2*int((nf+1)/2) * (W/nf + 0.18u)' ps='2*int((nf+2)/2) * (W/nf + 0.18u)' nrd='0.18u / W' nrs='0.18u / W'
+ sa=0 sb=0 sd=0 m=1
XM3[1] pre_divb reference AVDD AVDD pfet_03v3 L=0.28u W=0.9u nf=1 ad='int((nf+1)/2) * W/nf * 0.18u' as='int((nf+2)/2) * W/nf * 0.18u'
+ pd='2*int((nf+1)/2) * (W/nf + 0.18u)' ps='2*int((nf+2)/2) * (W/nf + 0.18u)' nrd='0.18u / W' nrs='0.18u / W'
+ sa=0 sb=0 sd=0 m=1
XM4[0] pre_divb reference GND GND nfet_03v3 L=0.28u W=0.3u nf=1 ad='int((nf+1)/2) * W/nf * 0.18u' as='int((nf+2)/2) * W/nf * 0.18u'
+ pd='2*int((nf+1)/2) * (W/nf + 0.18u)' ps='2*int((nf+2)/2) * (W/nf + 0.18u)' nrd='0.18u / W' nrs='0.18u / W'
+ sa=0 sb=0 sd=0 m=1
XM4[1] pre_divb reference GND GND nfet_03v3 L=0.28u W=0.3u nf=1 ad='int((nf+1)/2) * W/nf * 0.18u' as='int((nf+2)/2) * W/nf * 0.18u'
+ pd='2*int((nf+1)/2) * (W/nf + 0.18u)' ps='2*int((nf+2)/2) * (W/nf + 0.18u)' nrd='0.18u / W' nrs='0.18u / W'
+ sa=0 sb=0 sd=0 m=1
V3 rst 0 PWL(0 0 10n 0 10.1n 3.3)
XM31 Sb1 S1 AVDD AVDD pfet_03v3 L=0.28u W=0.9u nf=1 ad='int((nf+1)/2) * W/nf * 0.18u' as='int((nf+2)/2) * W/nf * 0.18u'
+ pd='2*int((nf+1)/2) * (W/nf + 0.18u)' ps='2*int((nf+2)/2) * (W/nf + 0.18u)' nrd='0.18u / W' nrs='0.18u / W'
+ sa=0 sb=0 sd=0 m=1
XM32 Sb2 S2 AVDD AVDD pfet_03v3 L=0.28u W=0.9u nf=1 ad='int((nf+1)/2) * W/nf * 0.18u' as='int((nf+2)/2) * W/nf * 0.18u'
+ pd='2*int((nf+1)/2) * (W/nf + 0.18u)' ps='2*int((nf+2)/2) * (W/nf + 0.18u)' nrd='0.18u / W' nrs='0.18u / W'
+ sa=0 sb=0 sd=0 m=1
XM33 Sb3 S3 AVDD AVDD pfet_03v3 L=0.28u W=0.9u nf=1 ad='int((nf+1)/2) * W/nf * 0.18u' as='int((nf+2)/2) * W/nf * 0.18u'
+ pd='2*int((nf+1)/2) * (W/nf + 0.18u)' ps='2*int((nf+2)/2) * (W/nf + 0.18u)' nrd='0.18u / W' nrs='0.18u / W'
+ sa=0 sb=0 sd=0 m=1
XM34 Sb4 S4 AVDD AVDD pfet_03v3 L=0.28u W=0.9u nf=1 ad='int((nf+1)/2) * W/nf * 0.18u' as='int((nf+2)/2) * W/nf * 0.18u'
+ pd='2*int((nf+1)/2) * (W/nf + 0.18u)' ps='2*int((nf+2)/2) * (W/nf + 0.18u)' nrd='0.18u / W' nrs='0.18u / W'
+ sa=0 sb=0 sd=0 m=1
XM41 Sb1 S1 AVSS AVSS nfet_03v3 L=0.28u W=0.3u nf=1 ad='int((nf+1)/2) * W/nf * 0.18u' as='int((nf+2)/2) * W/nf * 0.18u'
+ pd='2*int((nf+1)/2) * (W/nf + 0.18u)' ps='2*int((nf+2)/2) * (W/nf + 0.18u)' nrd='0.18u / W' nrs='0.18u / W'
+ sa=0 sb=0 sd=0 m=1
XM42 Sb2 S2 AVSS AVSS nfet_03v3 L=0.28u W=0.3u nf=1 ad='int((nf+1)/2) * W/nf * 0.18u' as='int((nf+2)/2) * W/nf * 0.18u'
+ pd='2*int((nf+1)/2) * (W/nf + 0.18u)' ps='2*int((nf+2)/2) * (W/nf + 0.18u)' nrd='0.18u / W' nrs='0.18u / W'
+ sa=0 sb=0 sd=0 m=1
XM43 Sb3 S3 AVSS AVSS nfet_03v3 L=0.28u W=0.3u nf=1 ad='int((nf+1)/2) * W/nf * 0.18u' as='int((nf+2)/2) * W/nf * 0.18u'
+ pd='2*int((nf+1)/2) * (W/nf + 0.18u)' ps='2*int((nf+2)/2) * (W/nf + 0.18u)' nrd='0.18u / W' nrs='0.18u / W'
+ sa=0 sb=0 sd=0 m=1
XM44 Sb4 S4 AVSS AVSS nfet_03v3 L=0.28u W=0.3u nf=1 ad='int((nf+1)/2) * W/nf * 0.18u' as='int((nf+2)/2) * W/nf * 0.18u'
+ pd='2*int((nf+1)/2) * (W/nf + 0.18u)' ps='2*int((nf+2)/2) * (W/nf + 0.18u)' nrd='0.18u / W' nrs='0.18u / W'
+ sa=0 sb=0 sd=0 m=1
**.ends
.end
